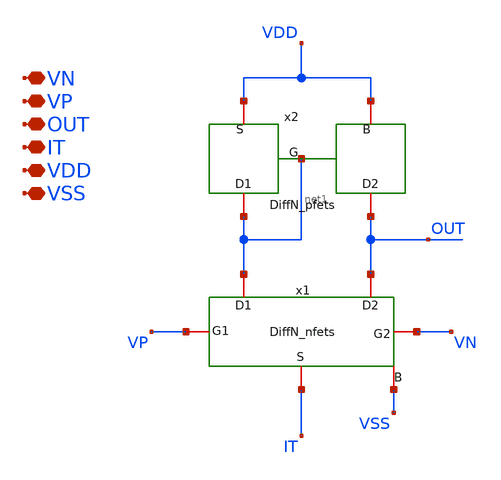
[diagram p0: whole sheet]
** sch_path: TIA_Filter/PseudoResistor/DiffN_net.sch
**.subckt DiffN_net VN VP OUT IT VDD VSS
*.iopin VN
*.iopin VP
*.iopin OUT
*.iopin IT
*.iopin VDD
*.iopin VSS
x1 net1 OUT VP VN IT VSS DiffN_nfets
x2 net1 OUT net1 VDD VDD DiffN_pfets
**.ends
.end
